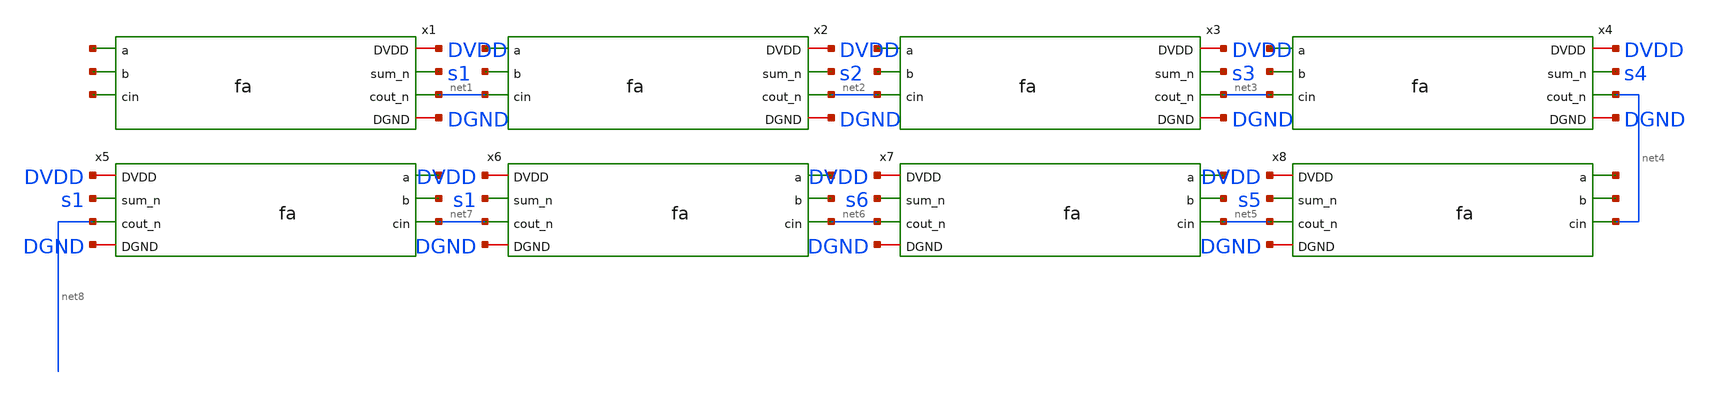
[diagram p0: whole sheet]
** sch_path: tut6/rca/rca8b.sch
**.subckt rca8b
x1 DVDD net9 net10 net11 s1 net1 DGND fa
x2 DVDD net12 net13 net1 s2 net2 DGND fa
x3 DVDD net14 net15 net2 s3 net3 DGND fa
x4 DVDD net16 net17 net3 s4 net4 DGND fa
x5 DVDD net18 net19 net7 s1 net8 DGND fa
x6 DVDD net20 net21 net6 s1 net7 DGND fa
x7 DVDD net22 net23 net5 s6 net6 DGND fa
x8 DVDD net24 net25 net4 s5 net5 DGND fa
**.ends
.end
